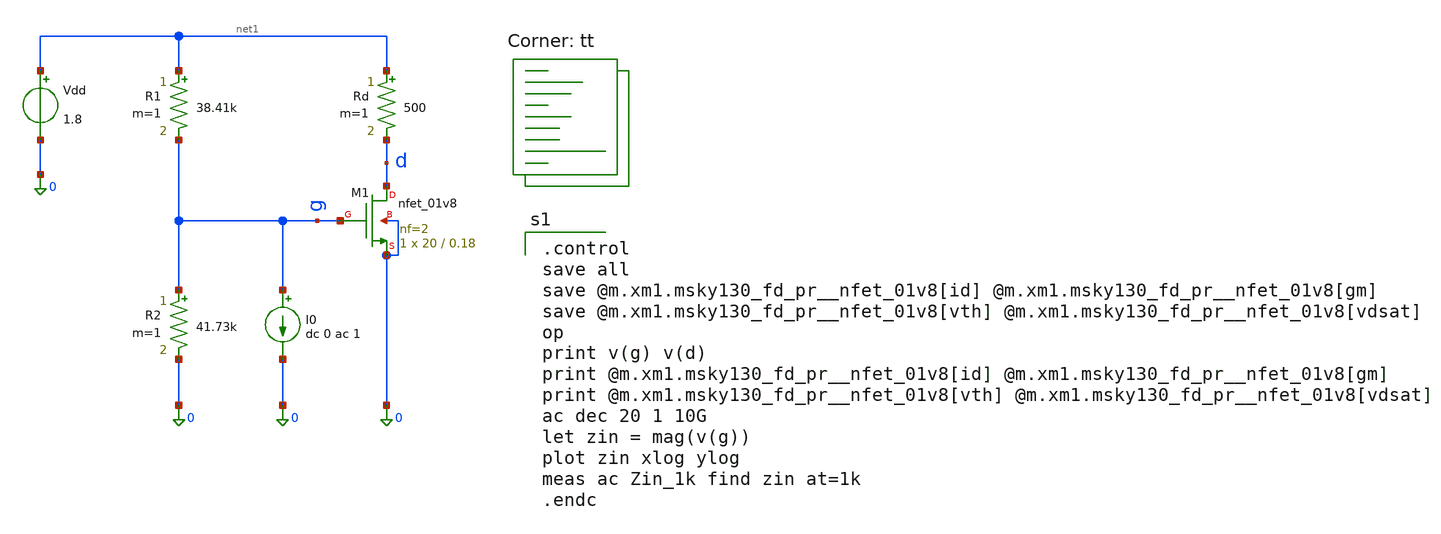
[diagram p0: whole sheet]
** sch_path: Homework 4 - Differential Pair Small Signal Gain/Simulations/ex1_final.sch
**.subckt ex1_final
XM1 d g 0 0 sky130_fd_pr__nfet_01v8 L=0.18 W=20 nf=2 ad='int((2 + 1)/2) * 20 / 2 * 0.29' as='int((2 + 2)/2) * 20 / 2 * 0.29'
+ pd='2*int((2 + 1)/2) * (20 / 2 + 0.29)' ps='2*int((2 + 2)/2) * (20 / 2 + 0.29)' nrd='0.29 / 20 ' nrs='0.29 / 20 '
+ sa=0 sb=0 sd=0 mult=1 m=1
Vdd net1 0 1.8
Rd net1 d 500 m=1
R1 net1 g 38.41k m=1
R2 g 0 41.73k m=1
I0 g 0 dc 0 ac 1
**** begin user architecture code
.lib $::SKYWATER_MODELS/sky130.lib.spice tt

.control
save all
save @m.xm1.msky130_fd_pr__nfet_01v8[id] @m.xm1.msky130_fd_pr__nfet_01v8[gm]
save @m.xm1.msky130_fd_pr__nfet_01v8[vth] @m.xm1.msky130_fd_pr__nfet_01v8[vdsat]
op
print v(g) v(d)
print @m.xm1.msky130_fd_pr__nfet_01v8[id] @m.xm1.msky130_fd_pr__nfet_01v8[gm]
print @m.xm1.msky130_fd_pr__nfet_01v8[vth] @m.xm1.msky130_fd_pr__nfet_01v8[vdsat]
ac dec 20 1 10G
let zin = mag(v(g))
plot zin xlog ylog
meas ac Zin_1k find zin at=1k
.endc

**** end user architecture code
**.ends
.end
